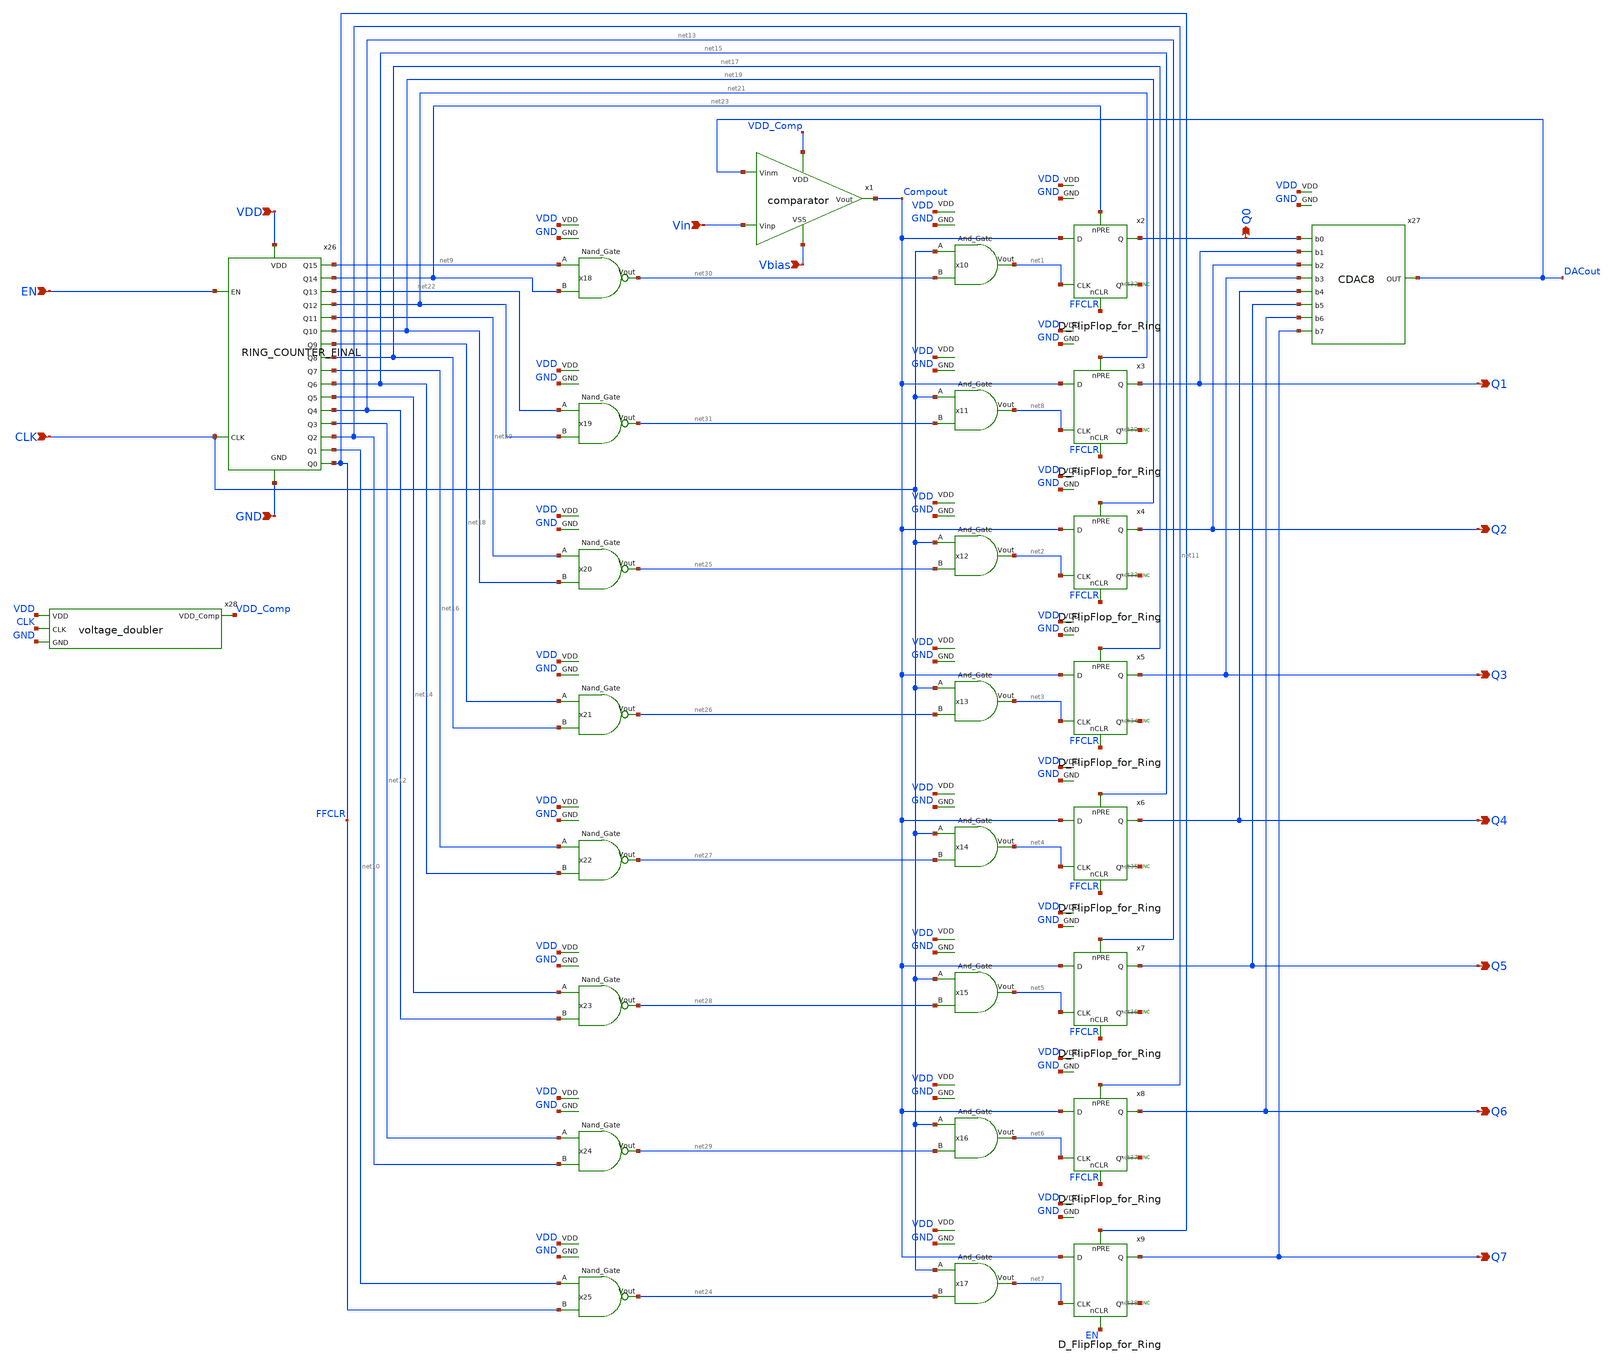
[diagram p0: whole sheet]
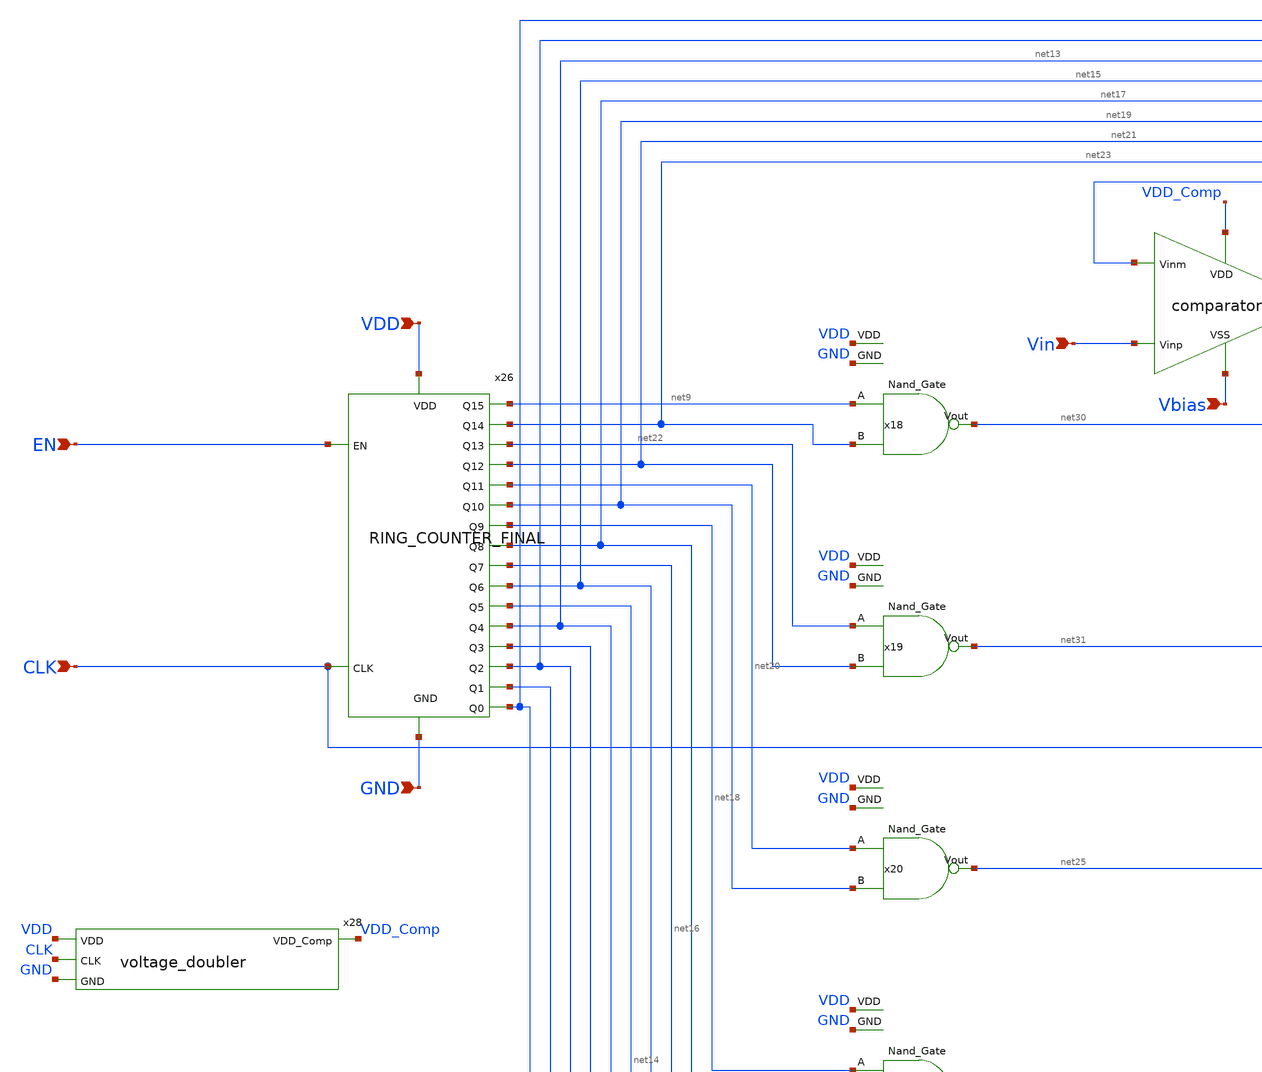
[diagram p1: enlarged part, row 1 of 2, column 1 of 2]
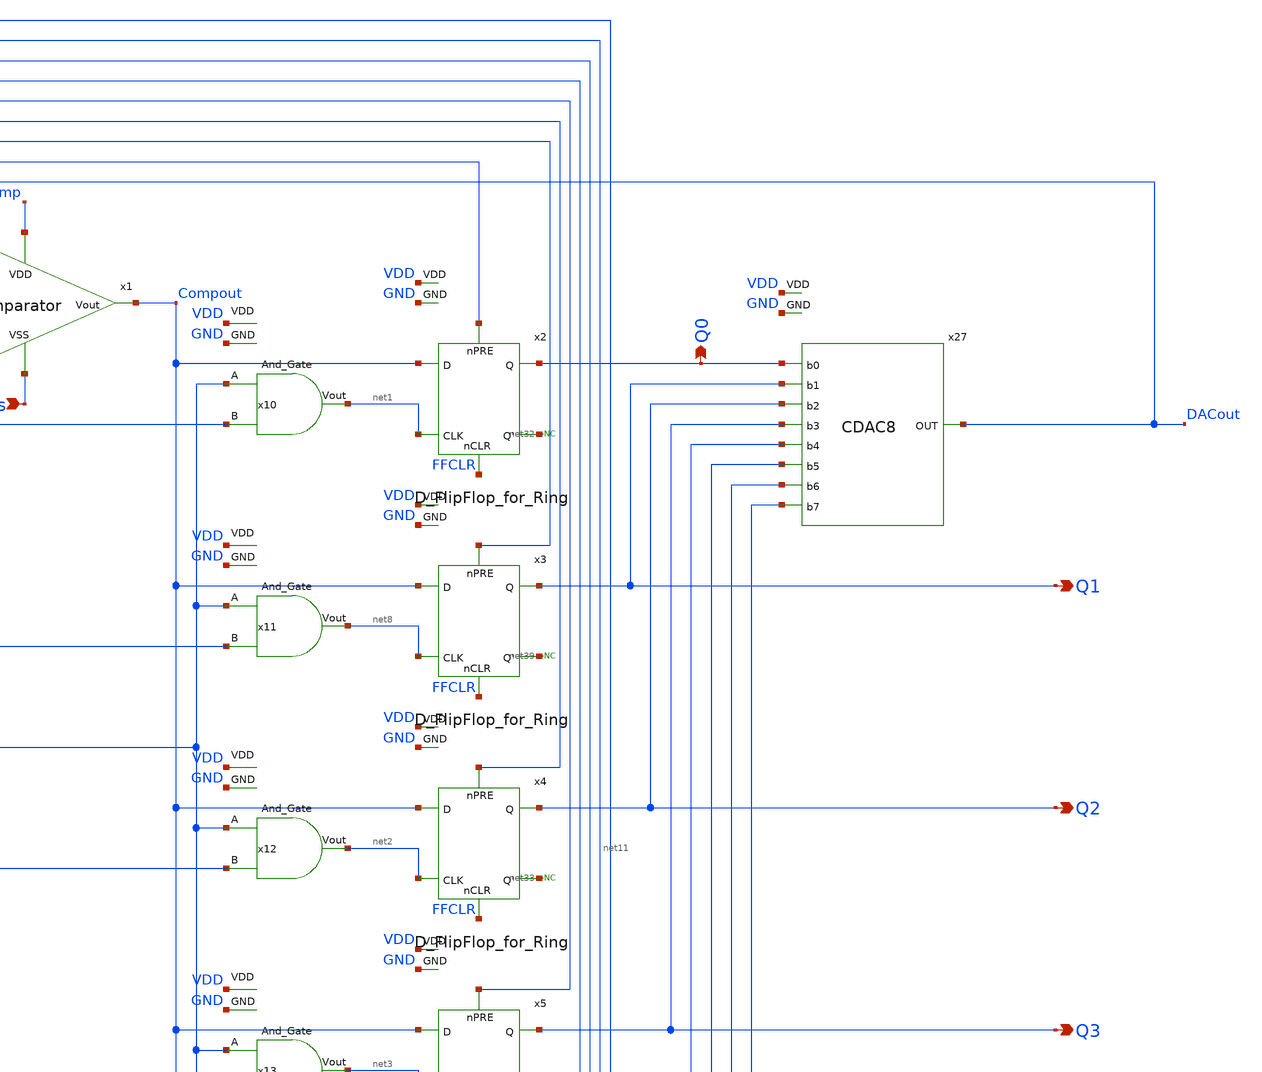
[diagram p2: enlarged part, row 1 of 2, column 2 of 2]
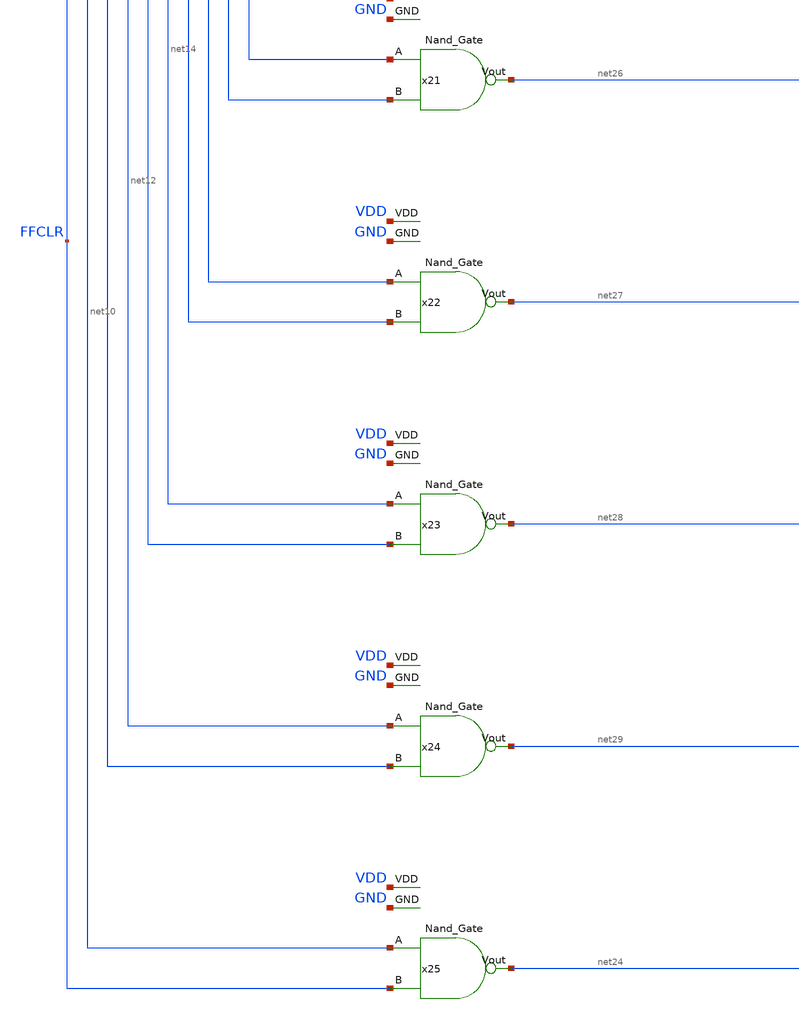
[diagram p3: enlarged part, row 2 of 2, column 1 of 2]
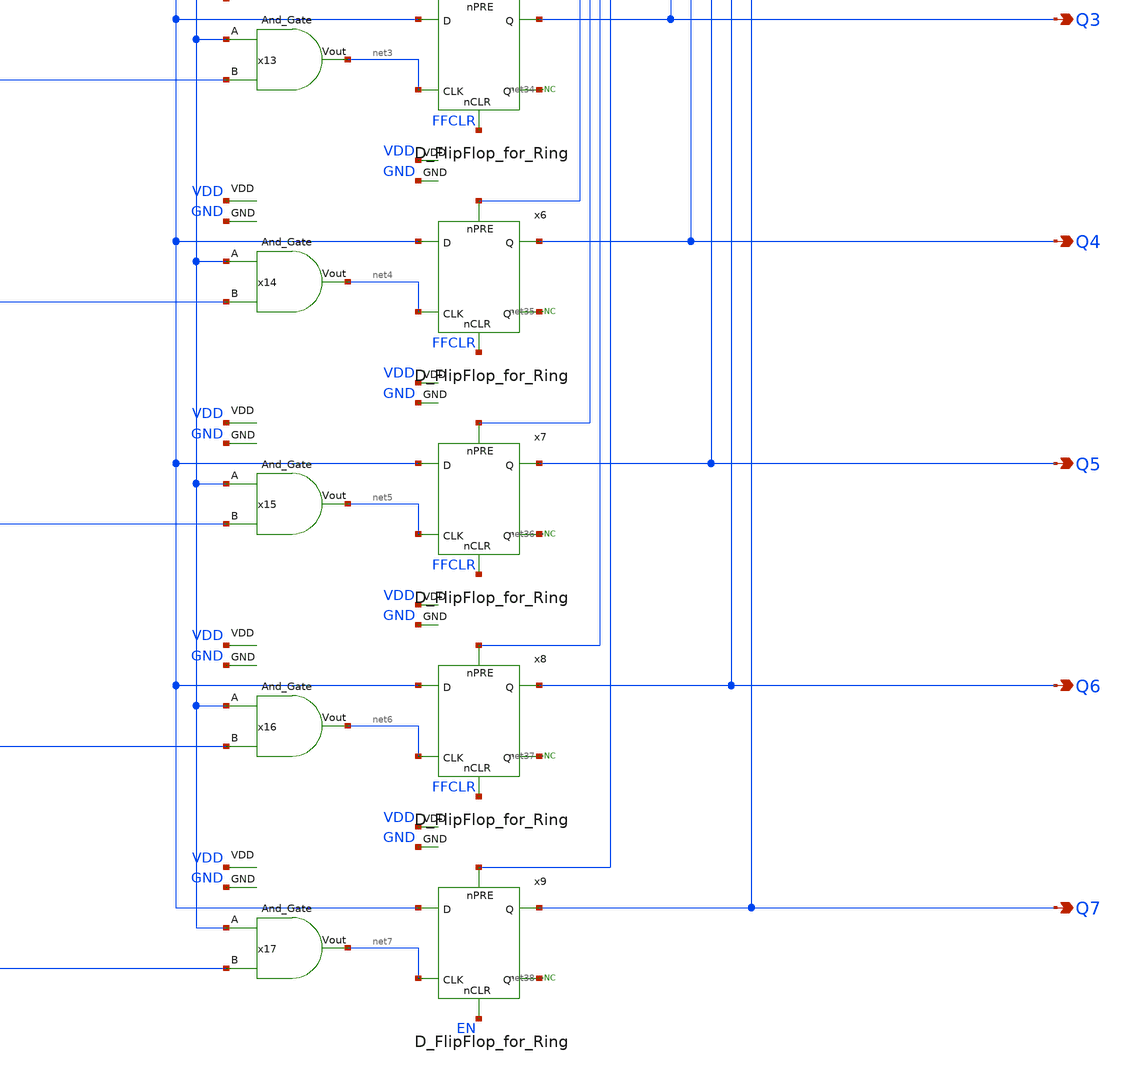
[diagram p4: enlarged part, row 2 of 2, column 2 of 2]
** sch_path: xschem/SAR-ADC-using-Sky130-PDK.sch
**.subckt SAR-ADC-using-Sky130-PDK EN CLK VDD Vin Q0 Q2 Q3 Q4 Q5 Q6 Q7 Q1 Vbias GND
*.ipin EN
*.ipin CLK
*.ipin VDD
*.ipin Vin
*.opin Q0
*.opin Q2
*.opin Q3
*.opin Q4
*.opin Q5
*.opin Q6
*.opin Q7
*.opin Q1
*.ipin Vbias
*.ipin GND
x2 net23 Compout Q0 net1 net32 FFCLR GND VDD D_FlipFlop_for_Ring
x4 net19 Compout Q2 net2 net33 FFCLR GND VDD D_FlipFlop_for_Ring
x5 net17 Compout Q3 net3 net34 FFCLR GND VDD D_FlipFlop_for_Ring
x6 net15 Compout Q4 net4 net35 FFCLR GND VDD D_FlipFlop_for_Ring
x7 net13 Compout Q5 net5 net36 FFCLR GND VDD D_FlipFlop_for_Ring
x8 net11 Compout Q6 net6 net37 FFCLR GND VDD D_FlipFlop_for_Ring
x9 FFCLR Compout Q7 net7 net38 EN GND VDD D_FlipFlop_for_Ring
x3 net21 Compout Q1 net8 net39 FFCLR GND VDD D_FlipFlop_for_Ring
x18 net9 net23 net30 GND VDD Nand_Gate
x19 net22 net21 net31 GND VDD Nand_Gate
x20 net20 net19 net25 GND VDD Nand_Gate
x21 net18 net17 net26 GND VDD Nand_Gate
x22 net16 net15 net27 GND VDD Nand_Gate
x23 net14 net13 net28 GND VDD Nand_Gate
x24 net12 net11 net29 GND VDD Nand_Gate
x25 net10 FFCLR net24 GND VDD Nand_Gate
x10 CLK net30 net1 GND VDD And_Gate
x11 CLK net31 net8 GND VDD And_Gate
x15 CLK net28 net5 GND VDD And_Gate
x12 CLK net25 net2 GND VDD And_Gate
x13 CLK net26 net3 GND VDD And_Gate
x14 CLK net27 net4 GND VDD And_Gate
x16 CLK net29 net6 GND VDD And_Gate
x17 CLK net24 net7 GND VDD And_Gate
x27 DACout Q7 Q6 Q5 Q4 Q3 Q2 Q1 Q0 GND VDD CDAC8
x1 Compout DACout Vin VDD_Comp Vbias comparator
x26 VDD net11 net9 net13 net14 net15 net16 net10 net18 net19 net20 net21 net22 net23 FFCLR net12
+ net17 CLK EN GND RING_COUNTER_FINAL
* noconn #net32
* noconn #net39
* noconn #net33
* noconn #net34
* noconn #net36
* noconn #net35
* noconn #net37
* noconn #net38
x28 VDD VDD_Comp CLK GND voltage_doubler
**.ends
.end
